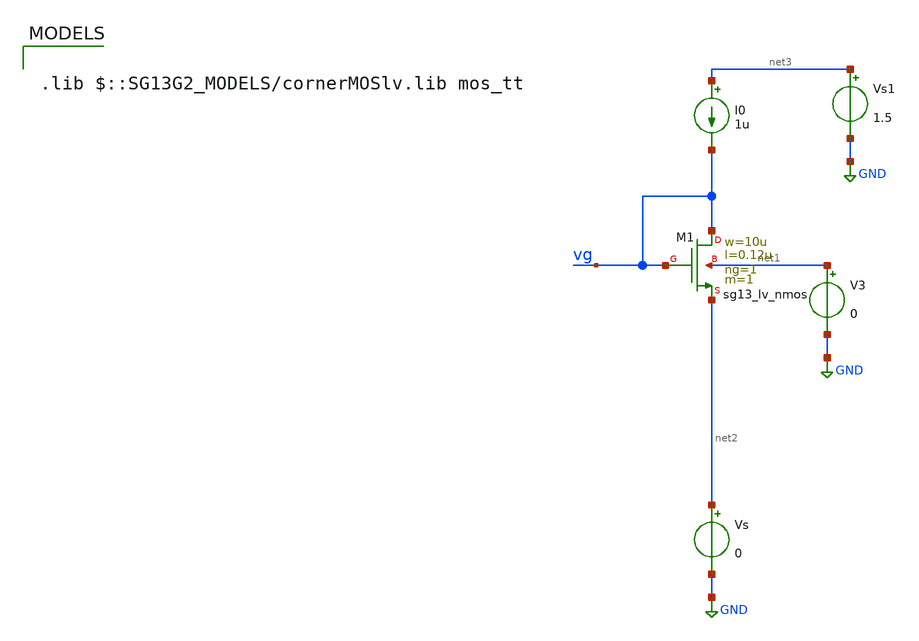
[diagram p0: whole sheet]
** sch_path: ihp_tutorials/nmos_op.sch
**.subckt nmos_op
V3 net1 GND 0
Vs net2 GND 0
XM1 vg vg net2 net1 sg13_lv_nmos w=10u l=0.12u ng=1 m=1 mm_ok=1
I0 net3 vg 1u
Vs1 net3 GND 1.5
**** begin user architecture code

.lib $::SG13G2_MODELS/cornerMOSlv.lib mos_tt



.option gmin = 1e-24

.control
pre_osdi ./psp103_nqs.osdi
save all

remzerovec
op
write nmos_op.raw

.endc



**** end user architecture code
**.ends
.GLOBAL GND
.end
